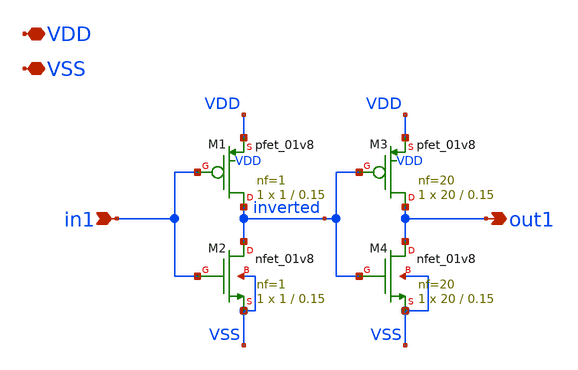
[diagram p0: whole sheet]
** sch_path: xschem/double_inverter.sch
**.subckt double_inverter VDD VSS in1 out1
*.iopin VDD
*.iopin VSS
*.ipin in1
*.opin out1
XM1 inverted in1 VDD VDD sky130_fd_pr__pfet_01v8 L=0.15 W=1 nf=1 ad='int((nf+1)/2) * W/nf * 0.29' as='int((nf+2)/2) * W/nf * 0.29'
+ pd='2*int((nf+1)/2) * (W/nf + 0.29)' ps='2*int((nf+2)/2) * (W/nf + 0.29)' nrd='0.29 / W' nrs='0.29 / W'
+ sa=0 sb=0 sd=0 mult=1 m=1
XM2 inverted in1 VSS VSS sky130_fd_pr__nfet_01v8 L=0.15 W=1 nf=1 ad='int((nf+1)/2) * W/nf * 0.29' as='int((nf+2)/2) * W/nf * 0.29'
+ pd='2*int((nf+1)/2) * (W/nf + 0.29)' ps='2*int((nf+2)/2) * (W/nf + 0.29)' nrd='0.29 / W' nrs='0.29 / W'
+ sa=0 sb=0 sd=0 mult=1 m=1
XM3 out1 inverted VDD VDD sky130_fd_pr__pfet_01v8 L=0.15 W=20 nf=20 ad='int((nf+1)/2) * W/nf * 0.29'
+ as='int((nf+2)/2) * W/nf * 0.29' pd='2*int((nf+1)/2) * (W/nf + 0.29)' ps='2*int((nf+2)/2) * (W/nf + 0.29)'
+ nrd='0.29 / W' nrs='0.29 / W' sa=0 sb=0 sd=0 mult=1 m=1
XM4 out1 inverted VSS VSS sky130_fd_pr__nfet_01v8 L=0.15 W=20 nf=20 ad='int((nf+1)/2) * W/nf * 0.29'
+ as='int((nf+2)/2) * W/nf * 0.29' pd='2*int((nf+1)/2) * (W/nf + 0.29)' ps='2*int((nf+2)/2) * (W/nf + 0.29)'
+ nrd='0.29 / W' nrs='0.29 / W' sa=0 sb=0 sd=0 mult=1 m=1
**.ends
.end
